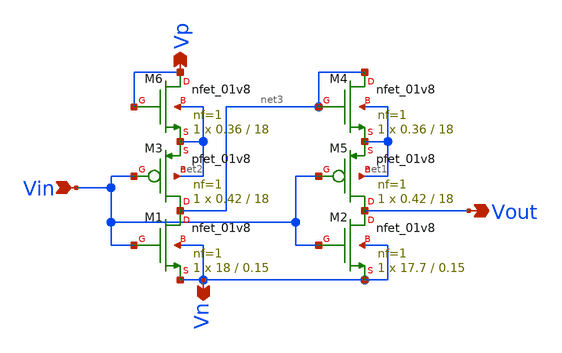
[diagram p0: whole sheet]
** sch_path: xschem/Vth_sch/Symbol/Inverter-th02.sch
**.subckt Inverter-th02 Vin Vout Vn Vp
*.ipin Vin
*.opin Vout
*.opin Vn
*.opin Vp
XM2 Vout Vin Vn Vn sky130_fd_pr__nfet_01v8 L=0.15 W=17.7 nf=1 ad='int((nf+1)/2) * W/nf * 0.29' as='int((nf+2)/2) * W/nf * 0.29'
+ pd='2*int((nf+1)/2) * (W/nf + 0.29)' ps='2*int((nf+2)/2) * (W/nf + 0.29)' nrd='0.29 / W' nrs='0.29 / W'
+ sa=0 sb=0 sd=0 mult=1 m=1
XM5 Vout Vin net1 net1 sky130_fd_pr__pfet_01v8 L=18 W=0.42 nf=1 ad='int((nf+1)/2) * W/nf * 0.29' as='int((nf+2)/2) * W/nf * 0.29'
+ pd='2*int((nf+1)/2) * (W/nf + 0.29)' ps='2*int((nf+2)/2) * (W/nf + 0.29)' nrd='0.29 / W' nrs='0.29 / W'
+ sa=0 sb=0 sd=0 mult=1 m=1
XM1 net3 Vin Vn Vn sky130_fd_pr__nfet_01v8 L=0.15 W=18 nf=1 ad='int((nf+1)/2) * W/nf * 0.29' as='int((nf+2)/2) * W/nf * 0.29'
+ pd='2*int((nf+1)/2) * (W/nf + 0.29)' ps='2*int((nf+2)/2) * (W/nf + 0.29)' nrd='0.29 / W' nrs='0.29 / W'
+ sa=0 sb=0 sd=0 mult=1 m=1
XM3 net3 Vin net2 net2 sky130_fd_pr__pfet_01v8 L=18 W=0.42 nf=1 ad='int((nf+1)/2) * W/nf * 0.29' as='int((nf+2)/2) * W/nf * 0.29'
+ pd='2*int((nf+1)/2) * (W/nf + 0.29)' ps='2*int((nf+2)/2) * (W/nf + 0.29)' nrd='0.29 / W' nrs='0.29 / W'
+ sa=0 sb=0 sd=0 mult=1 m=1
XM4 net3 net3 net1 net1 sky130_fd_pr__nfet_01v8 L=18 W=0.36 nf=1 ad='int((nf+1)/2) * W/nf * 0.29' as='int((nf+2)/2) * W/nf * 0.29'
+ pd='2*int((nf+1)/2) * (W/nf + 0.29)' ps='2*int((nf+2)/2) * (W/nf + 0.29)' nrd='0.29 / W' nrs='0.29 / W'
+ sa=0 sb=0 sd=0 mult=1 m=1
XM6 Vp Vp net2 net2 sky130_fd_pr__nfet_01v8 L=18 W=0.36 nf=1 ad='int((nf+1)/2) * W/nf * 0.29' as='int((nf+2)/2) * W/nf * 0.29'
+ pd='2*int((nf+1)/2) * (W/nf + 0.29)' ps='2*int((nf+2)/2) * (W/nf + 0.29)' nrd='0.29 / W' nrs='0.29 / W'
+ sa=0 sb=0 sd=0 mult=1 m=1
**.ends
.end
